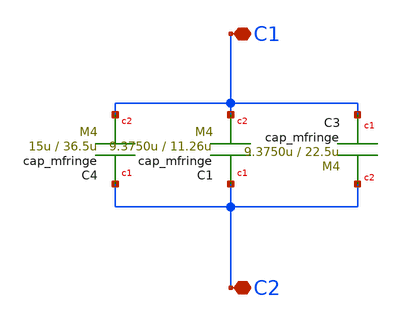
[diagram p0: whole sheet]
** sch_path: cfringe34x70.sch
**.subckt cfringe34x70 C1 C2
*.iopin C1
*.iopin C2
XC3 C1 C2 cap_mfringe w=9.3750u l=22.5u mmin=1 mmax=4
XC1 C2 C1 cap_mfringe w=9.3750u l=11.26u mmin=1 mmax=4
XC4 C2 C1 cap_mfringe w=15u l=36.5u mmin=1 mmax=4
**.ends
.end
